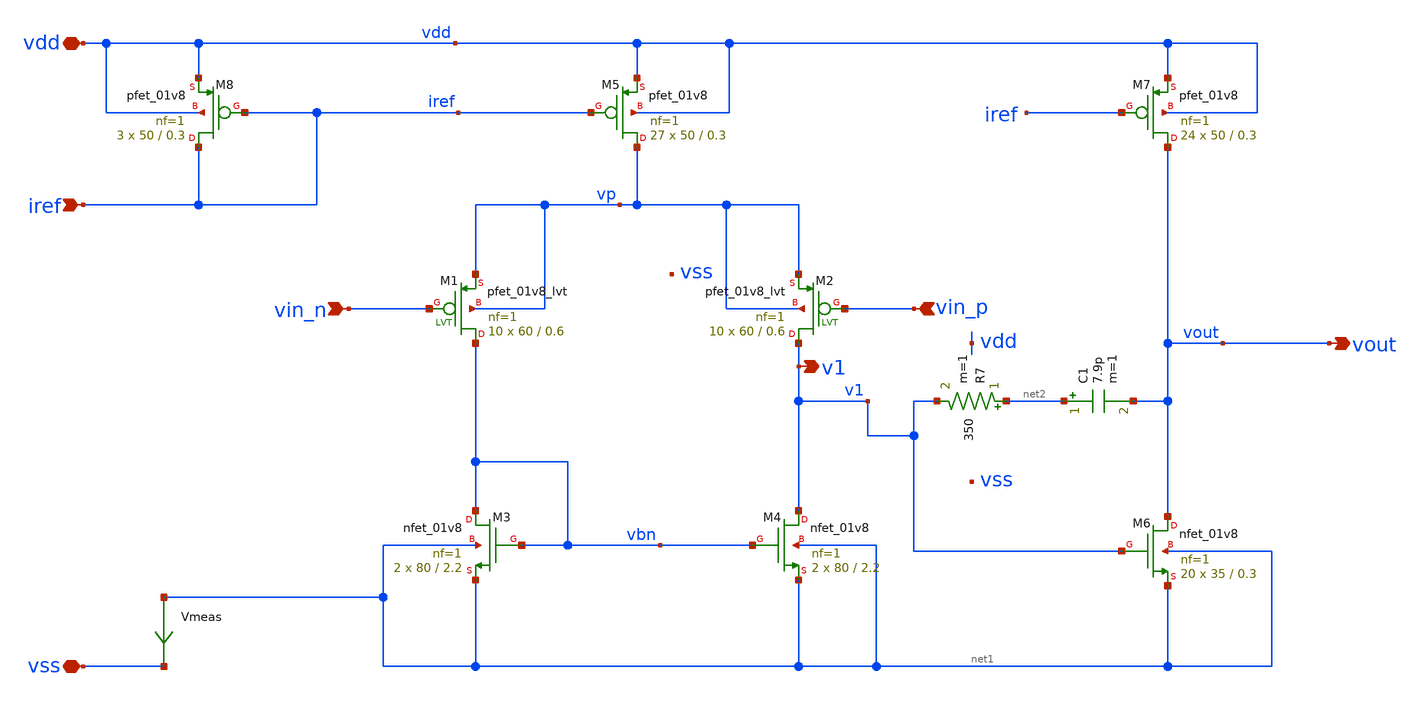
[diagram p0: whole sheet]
** sch_path: opamp/opamp.sch
**.subckt opamp vdd vss vin_n vin_p iref vout v1
*.iopin vdd
*.iopin vss
*.ipin vin_n
*.ipin vin_p
*.ipin iref
*.opin vout
*.opin v1
XM5 vp iref vdd vdd sky130_fd_pr__pfet_01v8 L=0.3 W=50 nf=1 ad='W * 0.29' as='W * 0.29' pd='2 * (W + 0.29)'
+ ps='2 * (W + 0.29)' nrd='0.29 / W' nrs='0.29 / W' sa=0 sb=0 sd=0 mult=27 m=27
XM7 vout iref vdd vdd sky130_fd_pr__pfet_01v8 L=0.3 W=50 nf=1 ad='W * 0.29' as='W * 0.29' pd='2 * (W + 0.29)'
+ ps='2 * (W + 0.29)' nrd='0.29 / W' nrs='0.29 / W' sa=0 sb=0 sd=0 mult=24 m=24
XM8 iref iref vdd vdd sky130_fd_pr__pfet_01v8 L=0.3 W=50 nf=1 ad='W * 0.29' as='W * 0.29' pd='2 * (W + 0.29)'
+ ps='2 * (W + 0.29)' nrd='0.29 / W' nrs='0.29 / W' sa=0 sb=0 sd=0 mult=3 m=3
XM1 vbn vin_n vp vp sky130_fd_pr__pfet_01v8_lvt L=0.6 W=60 nf=1 ad='int((nf+1)/2) * W/nf * 0.29' as='int((nf+2)/2) * W/nf * 0.29'
+ pd='2*int((nf+1)/2) * (W/nf + 0.29)' ps='2*int((nf+2)/2) * (W/nf + 0.29)' nrd='0.29 / W' nrs='0.29 / W'
+ sa=0 sb=0 sd=0 mult=10 m=10
XM2 v1 vin_p vp vp sky130_fd_pr__pfet_01v8_lvt L=0.6 W=60 nf=1 ad='int((nf+1)/2) * W/nf * 0.29' as='int((nf+2)/2) * W/nf * 0.29'
+ pd='2*int((nf+1)/2) * (W/nf + 0.29)' ps='2*int((nf+2)/2) * (W/nf + 0.29)' nrd='0.29 / W' nrs='0.29 / W'
+ sa=0 sb=0 sd=0 mult=10 m=10
C1 net2 vout 7.9p m=1
Vmeas net1 vss 0
.save i(vmeas)
R7 net2 v1 350 m=1
XM6 vout v1 net1 net1 sky130_fd_pr__nfet_01v8 L=0.3 W=35 nf=1 ad='W * 0.29' as='W * 0.29' pd='2 * (W + 0.29)'
+ ps='2 * (W + 0.29)' nrd='0.29 / W' nrs='0.29 / W' sa=0 sb=0 sd=0 mult=20 m=20
XM4 v1 vbn net1 net1 sky130_fd_pr__nfet_01v8 L=2.2 W=80 nf=1 ad='W * 0.29' as='W * 0.29' pd='2 * (W + 0.29)'
+ ps='2 * (W + 0.29)' nrd='0.29 / W' nrs='0.29 / W' sa=0 sb=0 sd=0 mult=2 m=2
XM3 vbn vbn net1 net1 sky130_fd_pr__nfet_01v8 L=2.2 W=80 nf=1 ad='W * 0.29' as='W * 0.29' pd='2 * (W + 0.29)'
+ ps='2 * (W + 0.29)' nrd='0.29 / W' nrs='0.29 / W' sa=0 sb=0 sd=0 mult=2 m=2
**.ends
.end
